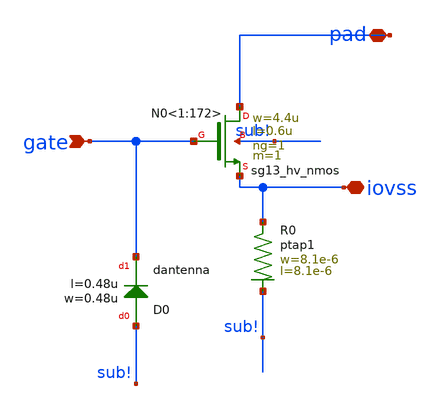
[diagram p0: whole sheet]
** sch_path: ihp-sg13g2/libs.ref/sg13g2_io/sch/xschem/sg13g2_Clamp_N43N43D4R.sch
**.subckt sg13g2_Clamp_N43N43D4R pad gate iovss
*.iopin pad
*.ipin gate
*.iopin iovss
XN0<1:172> pad gate iovss sub! sg13_hv_nmos w=4.4u l=0.6u ng=1 m=1 mm_ok=1
XD0 sub! gate dantenna l=0.48u w=0.48u
XR0 iovss sub! ptap1 R=9.999 w=8.1e-6 l=8.1e-6
**.ends
.end
